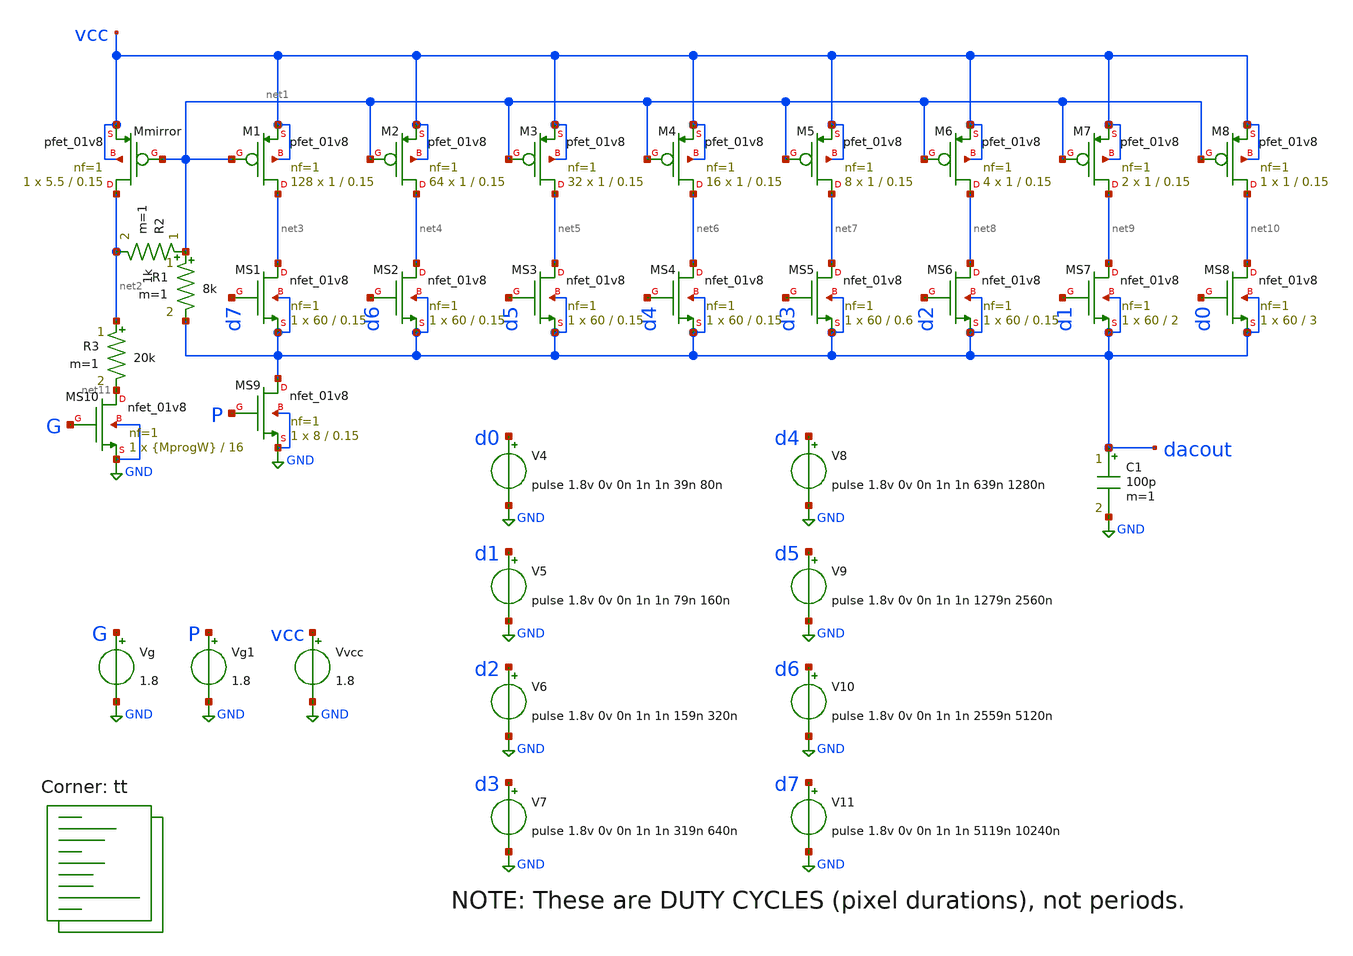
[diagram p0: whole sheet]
** sch_path: xschem/05c-res.sch
**.subckt 05c-res
Vvcc vcc GND 1.8
Vg G GND 1.8
XMmirror net2 net1 vcc vcc sky130_fd_pr__pfet_01v8 L=0.15 W=5.5 nf=1 ad='int((nf+1)/2) * W/nf * 0.29'
+ as='int((nf+2)/2) * W/nf * 0.29' pd='2*int((nf+1)/2) * (W/nf + 0.29)' ps='2*int((nf+2)/2) * (W/nf + 0.29)'
+ nrd='0.29 / W' nrs='0.29 / W' sa=0 sb=0 sd=0 mult=1 m=1
XM1 net3 net1 vcc vcc sky130_fd_pr__pfet_01v8 L=0.15 W=1 nf=1 ad='int((nf+1)/2) * W/nf * 0.29' as='int((nf+2)/2) * W/nf * 0.29'
+ pd='2*int((nf+1)/2) * (W/nf + 0.29)' ps='2*int((nf+2)/2) * (W/nf + 0.29)' nrd='0.29 / W' nrs='0.29 / W'
+ sa=0 sb=0 sd=0 mult=128 m=128
XM2 net4 net1 vcc vcc sky130_fd_pr__pfet_01v8 L=0.15 W=1 nf=1 ad='int((nf+1)/2) * W/nf * 0.29' as='int((nf+2)/2) * W/nf * 0.29'
+ pd='2*int((nf+1)/2) * (W/nf + 0.29)' ps='2*int((nf+2)/2) * (W/nf + 0.29)' nrd='0.29 / W' nrs='0.29 / W'
+ sa=0 sb=0 sd=0 mult=64 m=64
XM3 net5 net1 vcc vcc sky130_fd_pr__pfet_01v8 L=0.15 W=1 nf=1 ad='int((nf+1)/2) * W/nf * 0.29' as='int((nf+2)/2) * W/nf * 0.29'
+ pd='2*int((nf+1)/2) * (W/nf + 0.29)' ps='2*int((nf+2)/2) * (W/nf + 0.29)' nrd='0.29 / W' nrs='0.29 / W'
+ sa=0 sb=0 sd=0 mult=32 m=32
XM4 net6 net1 vcc vcc sky130_fd_pr__pfet_01v8 L=0.15 W=1 nf=1 ad='int((nf+1)/2) * W/nf * 0.29' as='int((nf+2)/2) * W/nf * 0.29'
+ pd='2*int((nf+1)/2) * (W/nf + 0.29)' ps='2*int((nf+2)/2) * (W/nf + 0.29)' nrd='0.29 / W' nrs='0.29 / W'
+ sa=0 sb=0 sd=0 mult=16 m=16
XM5 net7 net1 vcc vcc sky130_fd_pr__pfet_01v8 L=0.15 W=1 nf=1 ad='int((nf+1)/2) * W/nf * 0.29' as='int((nf+2)/2) * W/nf * 0.29'
+ pd='2*int((nf+1)/2) * (W/nf + 0.29)' ps='2*int((nf+2)/2) * (W/nf + 0.29)' nrd='0.29 / W' nrs='0.29 / W'
+ sa=0 sb=0 sd=0 mult=8 m=8
XM6 net8 net1 vcc vcc sky130_fd_pr__pfet_01v8 L=0.15 W=1 nf=1 ad='int((nf+1)/2) * W/nf * 0.29' as='int((nf+2)/2) * W/nf * 0.29'
+ pd='2*int((nf+1)/2) * (W/nf + 0.29)' ps='2*int((nf+2)/2) * (W/nf + 0.29)' nrd='0.29 / W' nrs='0.29 / W'
+ sa=0 sb=0 sd=0 mult=4 m=4
XM7 net9 net1 vcc vcc sky130_fd_pr__pfet_01v8 L=0.15 W=1 nf=1 ad='int((nf+1)/2) * W/nf * 0.29' as='int((nf+2)/2) * W/nf * 0.29'
+ pd='2*int((nf+1)/2) * (W/nf + 0.29)' ps='2*int((nf+2)/2) * (W/nf + 0.29)' nrd='0.29 / W' nrs='0.29 / W'
+ sa=0 sb=0 sd=0 mult=2 m=2
XM8 net10 net1 vcc vcc sky130_fd_pr__pfet_01v8 L=0.15 W=1 nf=1 ad='int((nf+1)/2) * W/nf * 0.29' as='int((nf+2)/2) * W/nf * 0.29'
+ pd='2*int((nf+1)/2) * (W/nf + 0.29)' ps='2*int((nf+2)/2) * (W/nf + 0.29)' nrd='0.29 / W' nrs='0.29 / W'
+ sa=0 sb=0 sd=0 mult=1 m=1
XMS1 net3 d7 dacout dacout sky130_fd_pr__nfet_01v8 L=0.15 W=60 nf=1 ad='int((nf+1)/2) * W/nf * 0.29'
+ as='int((nf+2)/2) * W/nf * 0.29' pd='2*int((nf+1)/2) * (W/nf + 0.29)' ps='2*int((nf+2)/2) * (W/nf + 0.29)'
+ nrd='0.29 / W' nrs='0.29 / W' sa=0 sb=0 sd=0 mult=1 m=1
XMS2 net4 d6 dacout dacout sky130_fd_pr__nfet_01v8 L=0.15 W=60 nf=1 ad='int((nf+1)/2) * W/nf * 0.29'
+ as='int((nf+2)/2) * W/nf * 0.29' pd='2*int((nf+1)/2) * (W/nf + 0.29)' ps='2*int((nf+2)/2) * (W/nf + 0.29)'
+ nrd='0.29 / W' nrs='0.29 / W' sa=0 sb=0 sd=0 mult=1 m=1
XMS3 net5 d5 dacout dacout sky130_fd_pr__nfet_01v8 L=0.15 W=60 nf=1 ad='int((nf+1)/2) * W/nf * 0.29'
+ as='int((nf+2)/2) * W/nf * 0.29' pd='2*int((nf+1)/2) * (W/nf + 0.29)' ps='2*int((nf+2)/2) * (W/nf + 0.29)'
+ nrd='0.29 / W' nrs='0.29 / W' sa=0 sb=0 sd=0 mult=1 m=1
XMS4 net6 d4 dacout dacout sky130_fd_pr__nfet_01v8 L=0.15 W=60 nf=1 ad='int((nf+1)/2) * W/nf * 0.29'
+ as='int((nf+2)/2) * W/nf * 0.29' pd='2*int((nf+1)/2) * (W/nf + 0.29)' ps='2*int((nf+2)/2) * (W/nf + 0.29)'
+ nrd='0.29 / W' nrs='0.29 / W' sa=0 sb=0 sd=0 mult=1 m=1
XMS5 net7 d3 dacout dacout sky130_fd_pr__nfet_01v8 L=0.6 W=60 nf=1 ad='int((nf+1)/2) * W/nf * 0.29' as='int((nf+2)/2) * W/nf * 0.29'
+ pd='2*int((nf+1)/2) * (W/nf + 0.29)' ps='2*int((nf+2)/2) * (W/nf + 0.29)' nrd='0.29 / W' nrs='0.29 / W'
+ sa=0 sb=0 sd=0 mult=1 m=1
XMS6 net8 d2 dacout dacout sky130_fd_pr__nfet_01v8 L=0.15 W=60 nf=1 ad='int((nf+1)/2) * W/nf * 0.29'
+ as='int((nf+2)/2) * W/nf * 0.29' pd='2*int((nf+1)/2) * (W/nf + 0.29)' ps='2*int((nf+2)/2) * (W/nf + 0.29)'
+ nrd='0.29 / W' nrs='0.29 / W' sa=0 sb=0 sd=0 mult=1 m=1
XMS7 net9 d1 dacout dacout sky130_fd_pr__nfet_01v8 L=2 W=60 nf=1 ad='int((nf+1)/2) * W/nf * 0.29' as='int((nf+2)/2) * W/nf * 0.29'
+ pd='2*int((nf+1)/2) * (W/nf + 0.29)' ps='2*int((nf+2)/2) * (W/nf + 0.29)' nrd='0.29 / W' nrs='0.29 / W'
+ sa=0 sb=0 sd=0 mult=1 m=1
XMS8 net10 d0 dacout dacout sky130_fd_pr__nfet_01v8 L=3 W=60 nf=1 ad='int((nf+1)/2) * W/nf * 0.29' as='int((nf+2)/2) * W/nf * 0.29'
+ pd='2*int((nf+1)/2) * (W/nf + 0.29)' ps='2*int((nf+2)/2) * (W/nf + 0.29)' nrd='0.29 / W' nrs='0.29 / W'
+ sa=0 sb=0 sd=0 mult=1 m=1
V4 d0 GND pulse 1.8v 0v 0n 1n 1n 39n 80n
V5 d1 GND pulse 1.8v 0v 0n 1n 1n 79n 160n
V6 d2 GND pulse 1.8v 0v 0n 1n 1n 159n 320n
V7 d3 GND pulse 1.8v 0v 0n 1n 1n 319n 640n
V8 d4 GND pulse 1.8v 0v 0n 1n 1n 639n 1280n
V9 d5 GND pulse 1.8v 0v 0n 1n 1n 1279n 2560n
V10 d6 GND pulse 1.8v 0v 0n 1n 1n 2559n 5120n
V11 d7 GND pulse 1.8v 0v 0n 1n 1n 5119n 10240n
XMS9 dacout P GND GND sky130_fd_pr__nfet_01v8 L=0.15 W=8 nf=1 ad='int((nf+1)/2) * W/nf * 0.29' as='int((nf+2)/2) * W/nf * 0.29'
+ pd='2*int((nf+1)/2) * (W/nf + 0.29)' ps='2*int((nf+2)/2) * (W/nf + 0.29)' nrd='0.29 / W' nrs='0.29 / W'
+ sa=0 sb=0 sd=0 mult=1 m=1
Vg1 P GND 1.8
C1 dacout GND 100p m=1
R1 net1 dacout 8k m=1
XMS10 net11 G GND GND sky130_fd_pr__nfet_01v8 L=16 W={MprogW} nf=1 ad='int((nf+1)/2) * W/nf * 0.29' as='int((nf+2)/2) * W/nf * 0.29'
+ pd='2*int((nf+1)/2) * (W/nf + 0.29)' ps='2*int((nf+2)/2) * (W/nf + 0.29)' nrd='0.29 / W' nrs='0.29 / W'
+ sa=0 sb=0 sd=0 mult=1 m=1
R2 net1 net2 1k m=1
R3 net2 net11 20k m=1
**** begin user architecture code



.param MprogW=1
.options savecurrents
.control

*  set temp=90
  save all
  tran 1n 12.8u
  write 05.raw v(dacout)

  set appendwrite
  alterparam MprogW=0.9
  reset
*  *set temp=10
  tran 1n 12.8u
  write 05.raw v(dacout)

  set appendwrite
  alterparam MprogW=0.75
  reset
*  *set temp=10
  tran 1n 12.8u
  write 05.raw v(dacout)

  set appendwrite
  alterparam MprogW=0.5
  reset
*  *set temp=10
  tran 1n 12.8u
  write 05.raw v(dacout)

.endc



.lib $::SKYWATER_MODELS/sky130.lib.spice tt
**** end user architecture code
**.ends
.GLOBAL GND
.end
